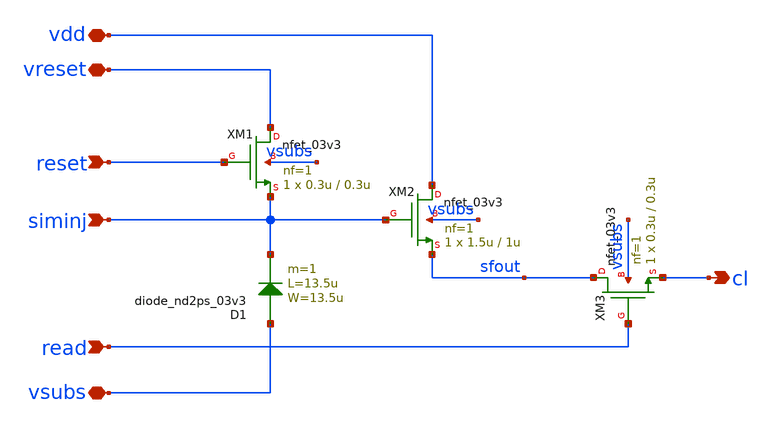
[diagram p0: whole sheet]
** sch_path: xschem/ip_pixel_nd2ps.sch
**.subckt ip_pixel_nd2ps vdd vsubs siminj reset read vreset cl
*.iopin vdd
*.iopin vsubs
*.ipin siminj
*.ipin reset
*.ipin read
*.iopin vreset
*.opin cl
XM1 vreset reset siminj vsubs nfet_03v3 L=0.3u W=0.3u nf=1 ad='int((nf+1)/2) * W/nf * 0.18u' as='int((nf+2)/2) * W/nf * 0.18u'
+ pd='2*int((nf+1)/2) * (W/nf + 0.18u)' ps='2*int((nf+2)/2) * (W/nf + 0.18u)' nrd='0.18u / W' nrs='0.18u / W'
+ sa=0 sb=0 sd=0 m=1
XM2 vdd siminj sfout vsubs nfet_03v3 L=1u W=1.5u nf=1 ad='int((nf+1)/2) * W/nf * 0.18u' as='int((nf+2)/2) * W/nf * 0.18u'
+ pd='2*int((nf+1)/2) * (W/nf + 0.18u)' ps='2*int((nf+2)/2) * (W/nf + 0.18u)' nrd='0.18u / W' nrs='0.18u / W'
+ sa=0 sb=0 sd=0 m=1
XM3 sfout read cl vsubs nfet_03v3 L=0.3u W=0.3u nf=1 ad='int((nf+1)/2) * W/nf * 0.18u' as='int((nf+2)/2) * W/nf * 0.18u'
+ pd='2*int((nf+1)/2) * (W/nf + 0.18u)' ps='2*int((nf+2)/2) * (W/nf + 0.18u)' nrd='0.18u / W' nrs='0.18u / W'
+ sa=0 sb=0 sd=0 m=1
D1 vsubs siminj diode_nd2ps_03v3 area='13.5u * 13.5u ' pj='2*13.5u + 2*13.5u ' m=1
**.ends
.end
